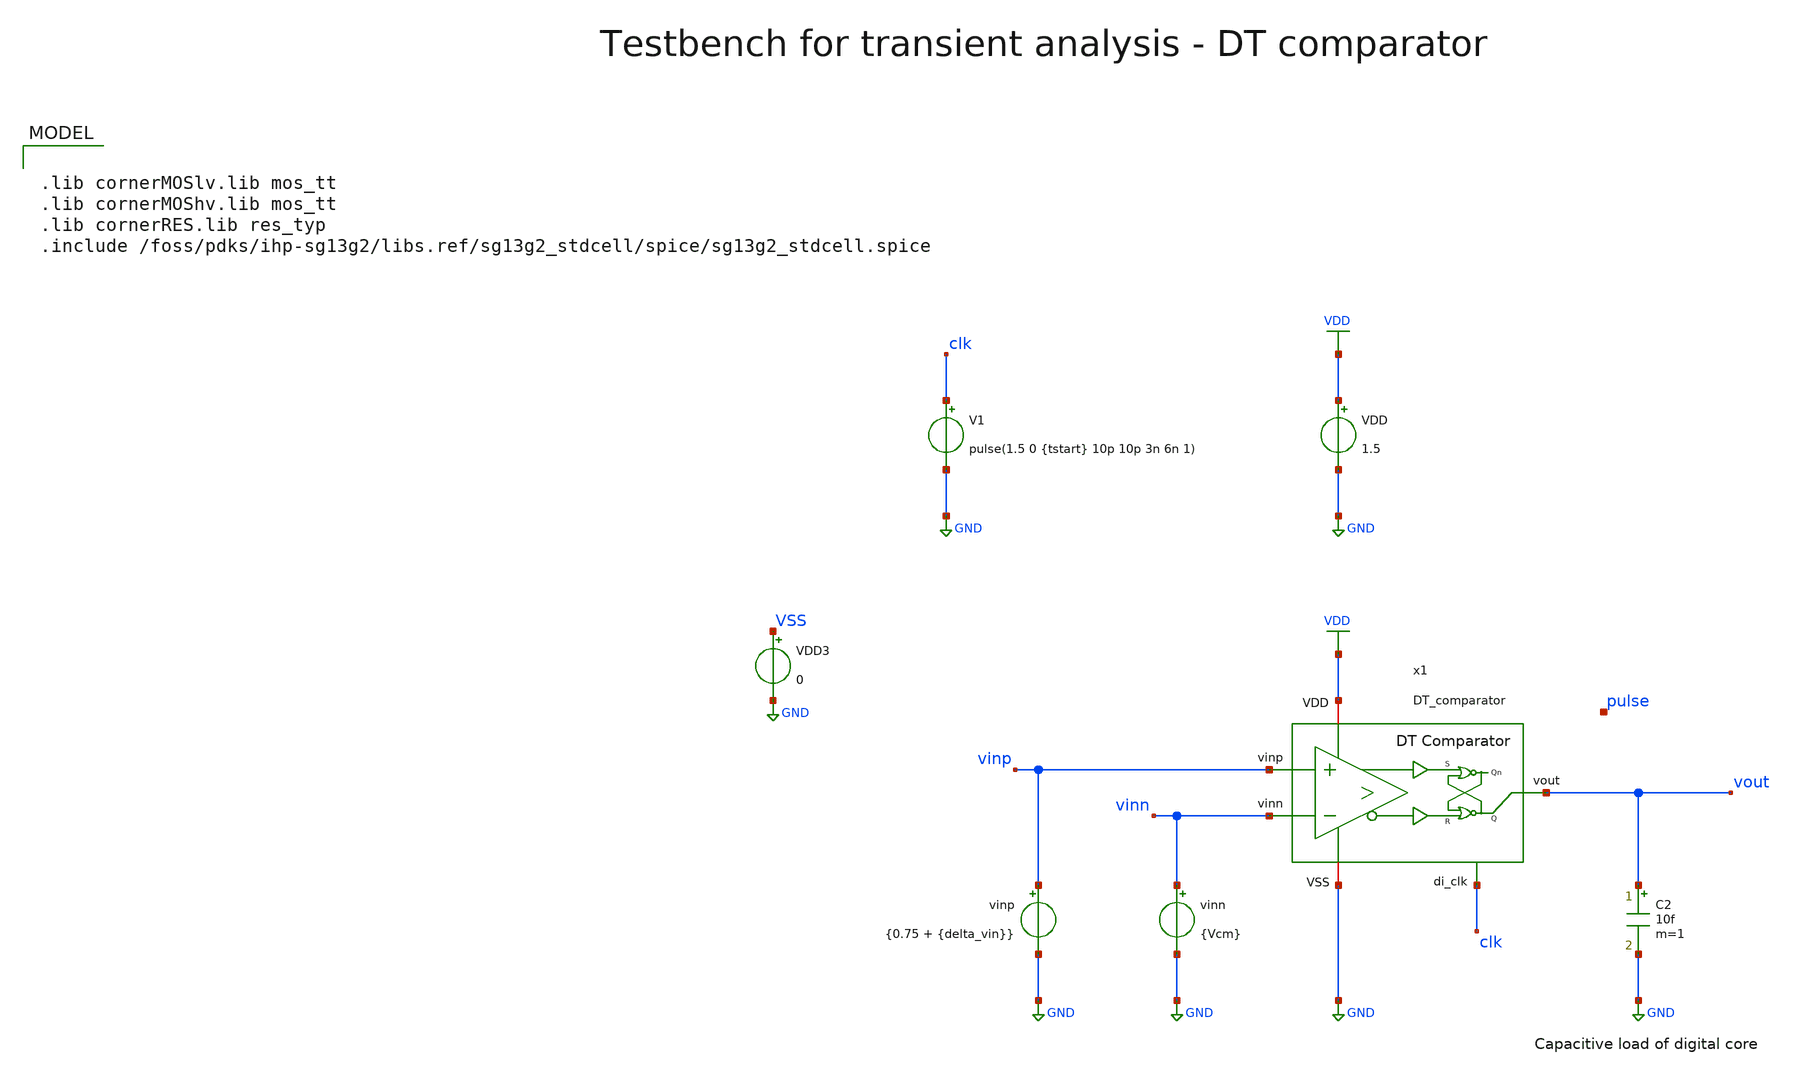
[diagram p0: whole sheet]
** sch_path: xschem/comparator/discrete_time/testbenches/DT_comparator_tb_tran.sch
**.subckt DT_comparator_tb_tran
VDD VDD GND 1.5
V1 clk GND pulse(1.5 0 {tstart} 10p 10p 3n 6n 1)
vinn vinn GND {Vcm}
vinp vinp GND {0.75 + {delta_vin}}
C2 vout GND 10f m=1
x1 VDD vinp vout vinn clk GND pulse DT_comparator
VDD3 VSS GND 0
**** begin user architecture code

.lib cornerMOSlv.lib mos_tt
.lib cornerMOShv.lib mos_tt
.lib cornerRES.lib res_typ
.include /foss/pdks/ihp-sg13g2/libs.ref/sg13g2_stdcell/spice/sg13g2_stdcell.spice



.param temp=27
.param fclk=8000000
.param fphi=62500
.param tstart=2n
.param delta_vin = 100m
.param Vcm=0.75
.csparam fclk=fclk
.csparam tstart=tstart
.options savecurrents reltol=1e-3 abstol=1e-12 gmin=1e-15
.ic v(vout) = 0
.control
save all

* Operating Point Analysis
op
remzerovec
write DT_comparator_tb_tran.raw
set appendwrite

* Transient Analysis
* tran 4p 20n
tran 40p 900n
*write DT_comparator_tb_tran.raw

* Measure vcpp_min & vcpn_min
*let tmeas = 1/fclk
*meas tran vcpp_min FIND v(x1.x1.vcpp) at=tmeas
*meas tran vcpn_min FIND v(x1.x1.vcpn) at=tmeas

* Measure Propagation Delay
* Time from clock rising edge to 90% VDD of vout
*let vout_limit = 0.9 * 1.5
*meas tran tcross WHEN v(vout)=vout_limit CROSS=1
*let tpd = tcross - tstart
*echo Propagation Delay $&tpd s

* Calculate Energy / Conversion
* i_int in As
* energy_conv in Ws = J
*let N = 1
*let t_conv = 150n
*meas tran i_int INTEG i(VDD) from=tstart to=t_conv
*let energy_conv = 1.5 * i_int / N

*let energy_conv_femto = energy_conv * 1e15
*echo Energy / Conversion $&energy_conv_femto fJ/conv

* Plotting
*plot v(clk) v(vinp) v(vinn)   v(x1.voutp_comp) v(x1.voutn_comp) v(vout)
*plot v(clk)  v(x1.voutp_comp) v(x1.voutn_comp) v(vout)
*plot i(VDD)
*plot v(clk)  {v(x1.x6.vx_n) +2} {v(vout) + 4} {v(x1.pulsen) + 6} {v(x1.x6.vx) + 8}  {v(x1.x6.READY) + 10}
plot v(x1.voutp_buf) {v(x1.voutn_buf)  + 2} {v(x1.x6.vx_n) + 4}  {v(pulse) + 8} {v(x1.x6.READY) + 10}
plot v(x1.voutp_comp) {v(x1.voutn_comp)  + 2} {v(x1.x6.vx_n) + 4}  {v(x1.x6.vx) + 8} {v(x1.x6.vxs) + 10}
* Writing Data
*set wr_singlescale
*set wr_vecnames
*let vs=x1.x1.vs
*let vcpp=x1.x1.vcpp
*let vcpn=x1.x1.vcpn
*let voutp_comp=x1.voutp_comp
*let voutn_comp=x1.voutn_comp
*wrdata /foss/designs/SG13G2_ATBS-ADC-main/python/plot_simulations/data/DT_comparator_tb_tran.txt
*+ v(clk) v(vinp) v(vinn) v(vs) v(vcpp) v(vcpn) v(voutp_comp) v(voutn_comp) v(vout)

*quit
.endc

**** end user architecture code
**.ends
.GLOBAL GND
.GLOBAL VDD
.end
